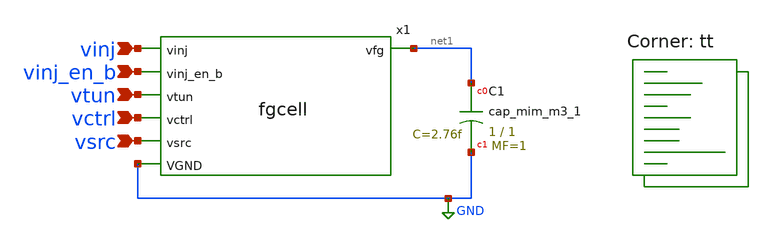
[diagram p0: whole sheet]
** sch_path: xschem/fgcell_MiM_cap_1_1.sch
**.subckt fgcell_MiM_cap_1_1 vinj vinj_en_b vtun vctrl vsrc
*.ipin vinj
*.ipin vinj_en_b
*.ipin vtun
*.ipin vctrl
*.ipin vsrc
x1 vinj vinj_en_b vtun vctrl vsrc GND net1 fgcell
XC1 net1 GND sky130_fd_pr__cap_mim_m3_1 W=1 L=1 MF=1 m=1
**** begin user architecture code
.lib $::SKYWATER_MODELS/sky130.lib.spice tt
**** end user architecture code
**.ends

* expanding   symbol:  fgcell.sym # of pins=7
** sym_path: xschem/fgcell.sym
** sch_path: xschem/fgcell.sch
.subckt fgcell vinj vinj_en_b vtun vctrl vsrc VGND vfg
*.ipin vinj
*.ipin vinj_en_b
*.ipin vtun
*.ipin vctrl
*.ipin vsrc
*.ipin VGND
*.opin vfg
XM1 vsrc vfg net1 vinj sky130_fd_pr__pfet_g5v0d10v5 L=0.5 W=1 nf=1 ad='int((nf+1)/2) * W/nf * 0.29' as='int((nf+2)/2) * W/nf * 0.29'
+ pd='2*int((nf+1)/2) * (W/nf + 0.29)' ps='2*int((nf+2)/2) * (W/nf + 0.29)' nrd='0.29 / W' nrs='0.29 / W'
+ sa=0 sb=0 sd=0 mult=1 m=1
XM2 net1 vinj_en_b vinj vinj sky130_fd_pr__pfet_g5v0d10v5 L=0.5 W=1 nf=1 ad='int((nf+1)/2) * W/nf * 0.29'
+ as='int((nf+2)/2) * W/nf * 0.29' pd='2*int((nf+1)/2) * (W/nf + 0.29)' ps='2*int((nf+2)/2) * (W/nf + 0.29)'
+ nrd='0.29 / W' nrs='0.29 / W' sa=0 sb=0 sd=0 mult=1 m=1
XC1 vfg vtun VGND sky130_fd_pr__cap_var_hvt W=1 L=0.5 VM=1 m=1
XM3 vctrl vfg vctrl vctrl sky130_fd_pr__pfet_g5v0d10v5 L=0.5 W=1 nf=1 ad='int((nf+1)/2) * W/nf * 0.29'
+ as='int((nf+2)/2) * W/nf * 0.29' pd='2*int((nf+1)/2) * (W/nf + 0.29)' ps='2*int((nf+2)/2) * (W/nf + 0.29)'
+ nrd='0.29 / W' nrs='0.29 / W' sa=0 sb=0 sd=0 mult=1 m=1
.ends

.GLOBAL GND
.end
